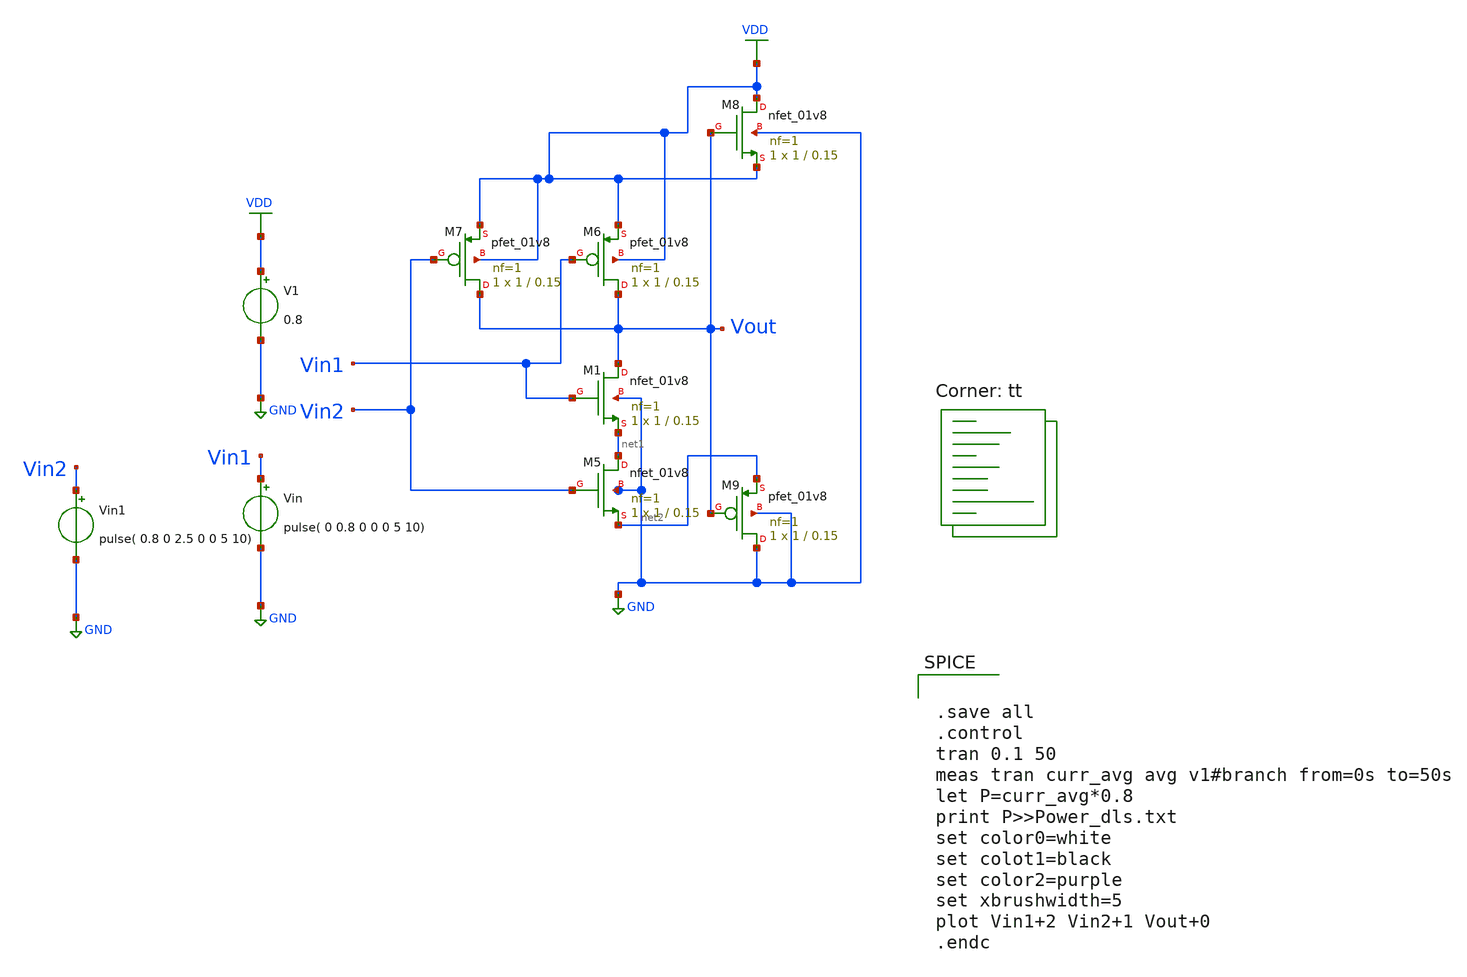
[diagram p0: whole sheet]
** sch_path: dls_nand.sch
**.subckt dls_nand
XM1 Vout Vin1 net1 GND sky130_fd_pr__nfet_01v8 L=0.15 W=1 nf=1 ad='int((nf+1)/2) * W/nf * 0.29' as='int((nf+2)/2) * W/nf * 0.29'
+ pd='2*int((nf+1)/2) * (W/nf + 0.29)' ps='2*int((nf+2)/2) * (W/nf + 0.29)' nrd='0.29 / W' nrs='0.29 / W'
+ sa=0 sb=0 sd=0 mult=1 m=1
V1 VDD GND 0.8
Vin Vin1 GND pulse( 0 0.8 0 0 0 5 10)
XM5 net1 Vin2 net2 GND sky130_fd_pr__nfet_01v8 L=0.15 W=1 nf=1 ad='int((nf+1)/2) * W/nf * 0.29' as='int((nf+2)/2) * W/nf * 0.29'
+ pd='2*int((nf+1)/2) * (W/nf + 0.29)' ps='2*int((nf+2)/2) * (W/nf + 0.29)' nrd='0.29 / W' nrs='0.29 / W'
+ sa=0 sb=0 sd=0 mult=1 m=1
XM6 Vout Vin1 VDD VDD sky130_fd_pr__pfet_01v8 L=0.15 W=1 nf=1 ad='int((nf+1)/2) * W/nf * 0.29' as='int((nf+2)/2) * W/nf * 0.29'
+ pd='2*int((nf+1)/2) * (W/nf + 0.29)' ps='2*int((nf+2)/2) * (W/nf + 0.29)' nrd='0.29 / W' nrs='0.29 / W'
+ sa=0 sb=0 sd=0 mult=1 m=1
XM7 Vout Vin2 VDD VDD sky130_fd_pr__pfet_01v8 L=0.15 W=1 nf=1 ad='int((nf+1)/2) * W/nf * 0.29' as='int((nf+2)/2) * W/nf * 0.29'
+ pd='2*int((nf+1)/2) * (W/nf + 0.29)' ps='2*int((nf+2)/2) * (W/nf + 0.29)' nrd='0.29 / W' nrs='0.29 / W'
+ sa=0 sb=0 sd=0 mult=1 m=1
XM8 VDD Vout VDD GND sky130_fd_pr__nfet_01v8 L=0.15 W=1 nf=1 ad='int((nf+1)/2) * W/nf * 0.29' as='int((nf+2)/2) * W/nf * 0.29'
+ pd='2*int((nf+1)/2) * (W/nf + 0.29)' ps='2*int((nf+2)/2) * (W/nf + 0.29)' nrd='0.29 / W' nrs='0.29 / W'
+ sa=0 sb=0 sd=0 mult=1 m=1
XM9 GND Vout net2 GND sky130_fd_pr__pfet_01v8 L=0.15 W=1 nf=1 ad='int((nf+1)/2) * W/nf * 0.29' as='int((nf+2)/2) * W/nf * 0.29'
+ pd='2*int((nf+1)/2) * (W/nf + 0.29)' ps='2*int((nf+2)/2) * (W/nf + 0.29)' nrd='0.29 / W' nrs='0.29 / W'
+ sa=0 sb=0 sd=0 mult=1 m=1
Vin1 Vin2 GND pulse( 0.8 0 2.5 0 0 5 10)
**** begin user architecture code
.lib $::SKYWATER_MODELS/sky130.lib.spice tt


.save all
.control
tran 0.1 50
meas tran curr_avg avg v1#branch from=0s to=50s
let P=curr_avg*0.8
print P>>Power_dls.txt
set color0=white
set colot1=black
set color2=purple
set xbrushwidth=5
plot Vin1+2 Vin2+1 Vout+0
.endc



**** end user architecture code
**.ends
.GLOBAL GND
.GLOBAL VDD
.end
